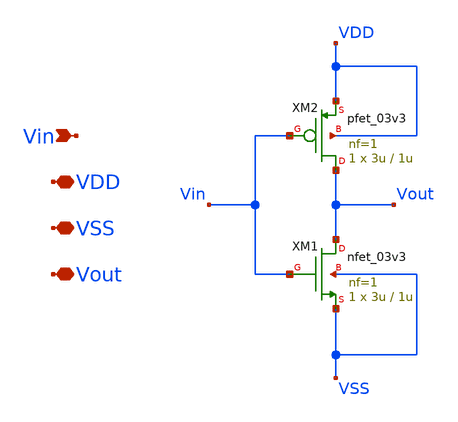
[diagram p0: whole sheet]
** sch_path: gf180_examples/inverter/xschem/inverter.sch
**.subckt inverter Vin VDD VSS Vout
*.ipin Vin
*.iopin VDD
*.iopin VSS
*.iopin Vout
XM1 Vout Vin VSS VSS nfet_03v3 L=1u W=3u nf=1 ad='int((nf+1)/2) * W/nf * 0.18u' as='int((nf+2)/2) * W/nf * 0.18u'
+ pd='2*int((nf+1)/2) * (W/nf + 0.18u)' ps='2*int((nf+2)/2) * (W/nf + 0.18u)' nrd='0.18u / W' nrs='0.18u / W'
+ sa=0 sb=0 sd=0 m=1
XM2 Vout Vin VDD VDD pfet_03v3 L=1u W=3u nf=1 ad='int((nf+1)/2) * W/nf * 0.18u' as='int((nf+2)/2) * W/nf * 0.18u'
+ pd='2*int((nf+1)/2) * (W/nf + 0.18u)' ps='2*int((nf+2)/2) * (W/nf + 0.18u)' nrd='0.18u / W' nrs='0.18u / W'
+ sa=0 sb=0 sd=0 m=1
**.ends
.end
